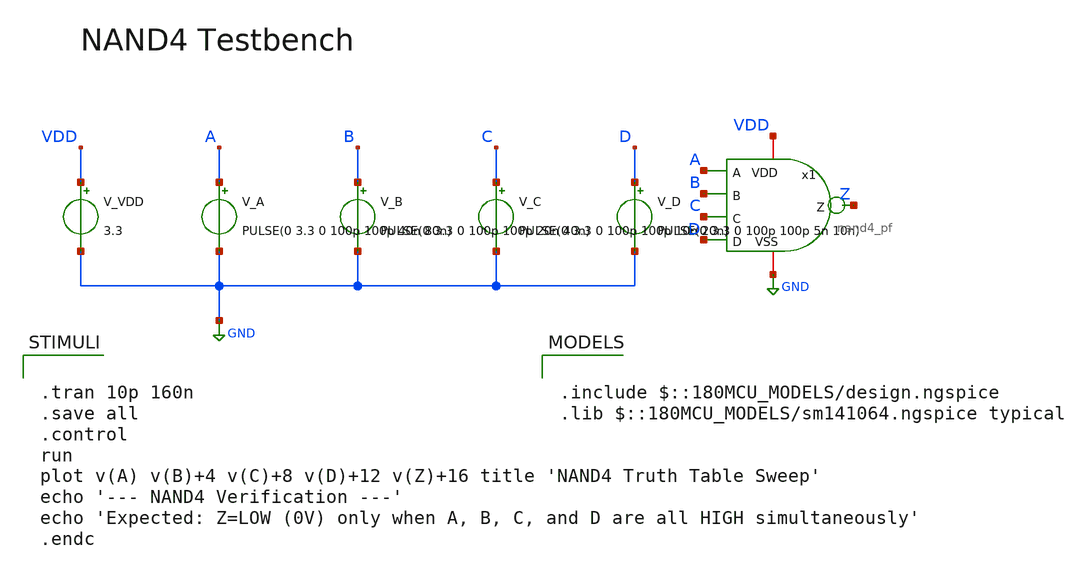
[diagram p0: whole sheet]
** sch_path: designs/libs/core_analog/pfd/nand4_tb.sch
**.subckt nand4_tb
V_VDD VDD GND 3.3
V_A A GND PULSE(0 3.3 0 100p 100p 40n 80n)
V_B B GND PULSE(0 3.3 0 100p 100p 20n 40n)
V_C C GND PULSE(0 3.3 0 100p 100p 10n 20n)
V_D D GND PULSE(0 3.3 0 100p 100p 5n 10n)
x1 VDD Z A B C D GND nand4_pf
**** begin user architecture code


.tran 10p 160n
.save all
.control
run
plot v(A) v(B)+4 v(C)+8 v(D)+12 v(Z)+16 title 'NAND4 Truth Table Sweep'
echo '--- NAND4 Verification ---'
echo 'Expected: Z=LOW (0V) only when A, B, C, and D are all HIGH simultaneously'
.endc



.include $::180MCU_MODELS/design.ngspice
.lib $::180MCU_MODELS/sm141064.ngspice typical

**** end user architecture code
**.ends

* expanding   symbol:  libs/core_analog/pfd/nand4_pf.sym # of pins=7
** sym_path: designs/libs/core_analog/pfd/nand4_pf.sym
** sch_path: designs/libs/core_analog/pfd/nand4_pf.sch
.subckt nand4_pf VDD Z A B C D VSS
*.iopin VDD
*.iopin VSS
*.ipin A
*.ipin B
*.ipin C
*.ipin D
*.opin Z
XMp1 Z A VDD VDD pfet_03v3 L=0.28u W=1u nf=1 ad='int((nf+1)/2) * W/nf * 0.18u' as='int((nf+2)/2) * W/nf * 0.18u'
+ pd='2*int((nf+1)/2) * (W/nf + 0.18u)' ps='2*int((nf+2)/2) * (W/nf + 0.18u)' nrd='0.18u / W' nrs='0.18u / W'
+ sa=0 sb=0 sd=0 m=1
XMp2 Z B VDD VDD pfet_03v3 L=0.28u W=1u nf=1 ad='int((nf+1)/2) * W/nf * 0.18u' as='int((nf+2)/2) * W/nf * 0.18u'
+ pd='2*int((nf+1)/2) * (W/nf + 0.18u)' ps='2*int((nf+2)/2) * (W/nf + 0.18u)' nrd='0.18u / W' nrs='0.18u / W'
+ sa=0 sb=0 sd=0 m=1
XMp3 Z C VDD VDD pfet_03v3 L=0.28u W=1u nf=1 ad='int((nf+1)/2) * W/nf * 0.18u' as='int((nf+2)/2) * W/nf * 0.18u'
+ pd='2*int((nf+1)/2) * (W/nf + 0.18u)' ps='2*int((nf+2)/2) * (W/nf + 0.18u)' nrd='0.18u / W' nrs='0.18u / W'
+ sa=0 sb=0 sd=0 m=1
XMp4 Z D VDD VDD pfet_03v3 L=0.28u W=1u nf=1 ad='int((nf+1)/2) * W/nf * 0.18u' as='int((nf+2)/2) * W/nf * 0.18u'
+ pd='2*int((nf+1)/2) * (W/nf + 0.18u)' ps='2*int((nf+2)/2) * (W/nf + 0.18u)' nrd='0.18u / W' nrs='0.18u / W'
+ sa=0 sb=0 sd=0 m=1
XMn1 Z A net1 VSS nfet_03v3 L=0.28u W=2u nf=1 ad='int((nf+1)/2) * W/nf * 0.18u' as='int((nf+2)/2) * W/nf * 0.18u'
+ pd='2*int((nf+1)/2) * (W/nf + 0.18u)' ps='2*int((nf+2)/2) * (W/nf + 0.18u)' nrd='0.18u / W' nrs='0.18u / W'
+ sa=0 sb=0 sd=0 m=1
XMn2 net1 B net2 VSS nfet_03v3 L=0.28u W=2u nf=1 ad='int((nf+1)/2) * W/nf * 0.18u' as='int((nf+2)/2) * W/nf * 0.18u'
+ pd='2*int((nf+1)/2) * (W/nf + 0.18u)' ps='2*int((nf+2)/2) * (W/nf + 0.18u)' nrd='0.18u / W' nrs='0.18u / W'
+ sa=0 sb=0 sd=0 m=1
XMn3 net2 C net3 VSS nfet_03v3 L=0.28u W=2u nf=1 ad='int((nf+1)/2) * W/nf * 0.18u' as='int((nf+2)/2) * W/nf * 0.18u'
+ pd='2*int((nf+1)/2) * (W/nf + 0.18u)' ps='2*int((nf+2)/2) * (W/nf + 0.18u)' nrd='0.18u / W' nrs='0.18u / W'
+ sa=0 sb=0 sd=0 m=1
XMn4 net3 D VSS VSS nfet_03v3 L=0.28u W=2u nf=1 ad='int((nf+1)/2) * W/nf * 0.18u' as='int((nf+2)/2) * W/nf * 0.18u'
+ pd='2*int((nf+1)/2) * (W/nf + 0.18u)' ps='2*int((nf+2)/2) * (W/nf + 0.18u)' nrd='0.18u / W' nrs='0.18u / W'
+ sa=0 sb=0 sd=0 m=1
.ends

.GLOBAL GND
.end
